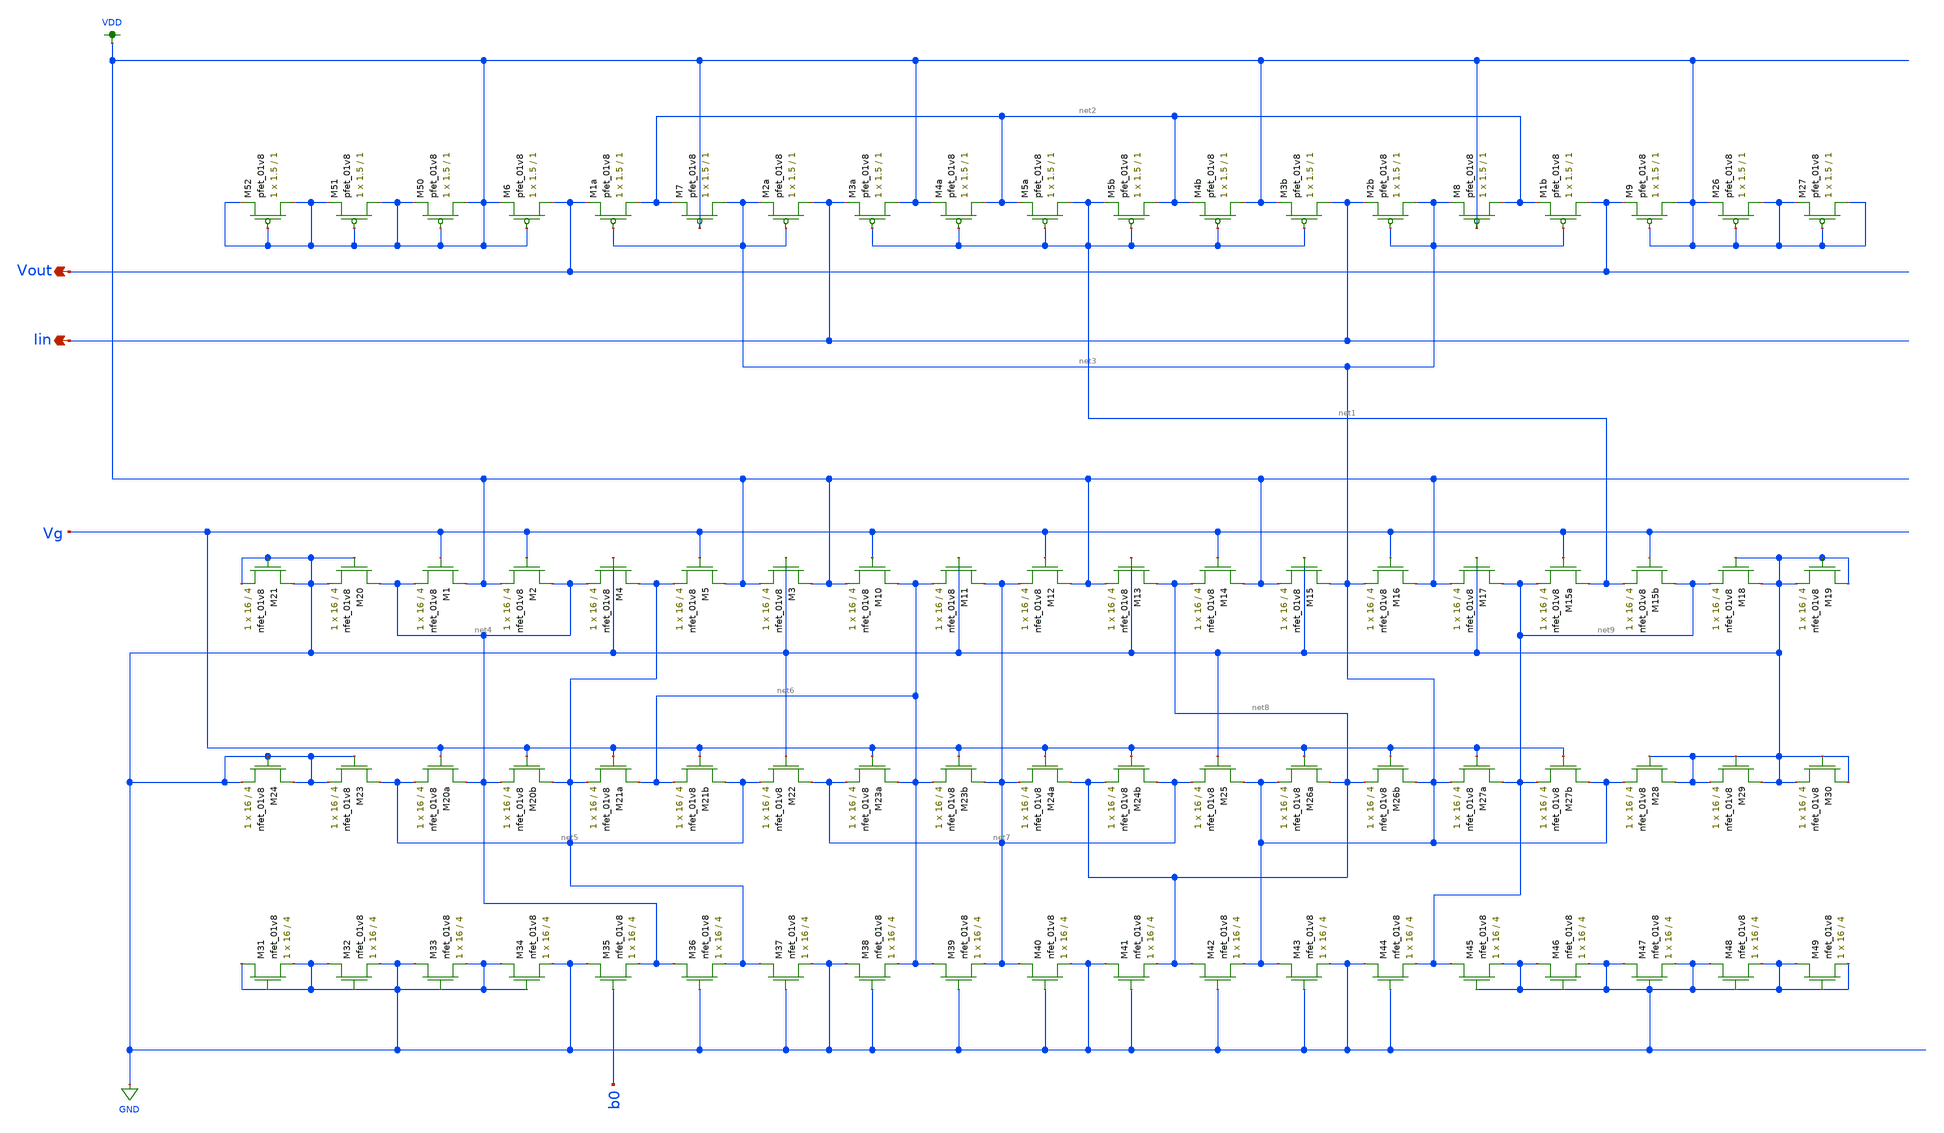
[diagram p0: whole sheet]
** sch_path: schematic/LDS/low-voltage_super-wilson.sch
**.subckt low-voltage_super-wilson Vout Iin
*.opin Vout
*.opin Iin
XM7 net3 VDD net2 VDD sky130_fd_pr__pfet_01v8 L=1 W=1.5 nf=1 ad='int((nf+1)/2) * W/nf * 0.29' as='int((nf+2)/2) * W/nf * 0.29'
+ pd='2*int((nf+1)/2) * (W/nf + 0.29)' ps='2*int((nf+2)/2) * (W/nf + 0.29)' nrd='0.29 / W' nrs='0.29 / W'
+ sa=0 sb=0 sd=0 mult=1 m=1
XM2a Iin net3 net3 VDD sky130_fd_pr__pfet_01v8 L=1 W=1.5 nf=1 ad='int((nf+1)/2) * W/nf * 0.29' as='int((nf+2)/2) * W/nf * 0.29'
+ pd='2*int((nf+1)/2) * (W/nf + 0.29)' ps='2*int((nf+2)/2) * (W/nf + 0.29)' nrd='0.29 / W' nrs='0.29 / W'
+ sa=0 sb=0 sd=0 mult=1 m=1
XM3a VDD net1 Iin VDD sky130_fd_pr__pfet_01v8 L=1 W=1.5 nf=1 ad='int((nf+1)/2) * W/nf * 0.29' as='int((nf+2)/2) * W/nf * 0.29'
+ pd='2*int((nf+1)/2) * (W/nf + 0.29)' ps='2*int((nf+2)/2) * (W/nf + 0.29)' nrd='0.29 / W' nrs='0.29 / W'
+ sa=0 sb=0 sd=0 mult=1 m=1
XM4a net2 net1 VDD VDD sky130_fd_pr__pfet_01v8 L=1 W=1.5 nf=1 ad='int((nf+1)/2) * W/nf * 0.29' as='int((nf+2)/2) * W/nf * 0.29'
+ pd='2*int((nf+1)/2) * (W/nf + 0.29)' ps='2*int((nf+2)/2) * (W/nf + 0.29)' nrd='0.29 / W' nrs='0.29 / W'
+ sa=0 sb=0 sd=0 mult=1 m=1
XM5a net1 net1 net2 VDD sky130_fd_pr__pfet_01v8 L=1 W=1.5 nf=1 ad='int((nf+1)/2) * W/nf * 0.29' as='int((nf+2)/2) * W/nf * 0.29'
+ pd='2*int((nf+1)/2) * (W/nf + 0.29)' ps='2*int((nf+2)/2) * (W/nf + 0.29)' nrd='0.29 / W' nrs='0.29 / W'
+ sa=0 sb=0 sd=0 mult=1 m=1
XM5b net2 net1 net1 VDD sky130_fd_pr__pfet_01v8 L=1 W=1.5 nf=1 ad='int((nf+1)/2) * W/nf * 0.29' as='int((nf+2)/2) * W/nf * 0.29'
+ pd='2*int((nf+1)/2) * (W/nf + 0.29)' ps='2*int((nf+2)/2) * (W/nf + 0.29)' nrd='0.29 / W' nrs='0.29 / W'
+ sa=0 sb=0 sd=0 mult=1 m=1
XM4b VDD net1 net2 VDD sky130_fd_pr__pfet_01v8 L=1 W=1.5 nf=1 ad='int((nf+1)/2) * W/nf * 0.29' as='int((nf+2)/2) * W/nf * 0.29'
+ pd='2*int((nf+1)/2) * (W/nf + 0.29)' ps='2*int((nf+2)/2) * (W/nf + 0.29)' nrd='0.29 / W' nrs='0.29 / W'
+ sa=0 sb=0 sd=0 mult=1 m=1
XM3b Iin net1 VDD VDD sky130_fd_pr__pfet_01v8 L=1 W=1.5 nf=1 ad='int((nf+1)/2) * W/nf * 0.29' as='int((nf+2)/2) * W/nf * 0.29'
+ pd='2*int((nf+1)/2) * (W/nf + 0.29)' ps='2*int((nf+2)/2) * (W/nf + 0.29)' nrd='0.29 / W' nrs='0.29 / W'
+ sa=0 sb=0 sd=0 mult=1 m=1
XM2b net3 net3 Iin VDD sky130_fd_pr__pfet_01v8 L=1 W=1.5 nf=1 ad='int((nf+1)/2) * W/nf * 0.29' as='int((nf+2)/2) * W/nf * 0.29'
+ pd='2*int((nf+1)/2) * (W/nf + 0.29)' ps='2*int((nf+2)/2) * (W/nf + 0.29)' nrd='0.29 / W' nrs='0.29 / W'
+ sa=0 sb=0 sd=0 mult=1 m=1
XM8 net2 VDD net3 VDD sky130_fd_pr__pfet_01v8 L=1 W=1.5 nf=1 ad='int((nf+1)/2) * W/nf * 0.29' as='int((nf+2)/2) * W/nf * 0.29'
+ pd='2*int((nf+1)/2) * (W/nf + 0.29)' ps='2*int((nf+2)/2) * (W/nf + 0.29)' nrd='0.29 / W' nrs='0.29 / W'
+ sa=0 sb=0 sd=0 mult=1 m=1
XM1a net2 net3 Vout VDD sky130_fd_pr__pfet_01v8 L=1 W=1.5 nf=1 ad='int((nf+1)/2) * W/nf * 0.29' as='int((nf+2)/2) * W/nf * 0.29'
+ pd='2*int((nf+1)/2) * (W/nf + 0.29)' ps='2*int((nf+2)/2) * (W/nf + 0.29)' nrd='0.29 / W' nrs='0.29 / W'
+ sa=0 sb=0 sd=0 mult=1 m=1
XM1b Vout net3 net2 VDD sky130_fd_pr__pfet_01v8 L=1 W=1.5 nf=1 ad='int((nf+1)/2) * W/nf * 0.29' as='int((nf+2)/2) * W/nf * 0.29'
+ pd='2*int((nf+1)/2) * (W/nf + 0.29)' ps='2*int((nf+2)/2) * (W/nf + 0.29)' nrd='0.29 / W' nrs='0.29 / W'
+ sa=0 sb=0 sd=0 mult=1 m=1
XM6 Vout VDD VDD VDD sky130_fd_pr__pfet_01v8 L=1 W=1.5 nf=1 ad='int((nf+1)/2) * W/nf * 0.29' as='int((nf+2)/2) * W/nf * 0.29'
+ pd='2*int((nf+1)/2) * (W/nf + 0.29)' ps='2*int((nf+2)/2) * (W/nf + 0.29)' nrd='0.29 / W' nrs='0.29 / W'
+ sa=0 sb=0 sd=0 mult=1 m=1
XM9 VDD VDD Vout VDD sky130_fd_pr__pfet_01v8 L=1 W=1.5 nf=1 ad='int((nf+1)/2) * W/nf * 0.29' as='int((nf+2)/2) * W/nf * 0.29'
+ pd='2*int((nf+1)/2) * (W/nf + 0.29)' ps='2*int((nf+2)/2) * (W/nf + 0.29)' nrd='0.29 / W' nrs='0.29 / W'
+ sa=0 sb=0 sd=0 mult=1 m=1
XM1 VDD Vg net4 GND sky130_fd_pr__nfet_01v8 L=4 W=16 nf=1 ad='int((nf+1)/2) * W/nf * 0.29' as='int((nf+2)/2) * W/nf * 0.29'
+ pd='2*int((nf+1)/2) * (W/nf + 0.29)' ps='2*int((nf+2)/2) * (W/nf + 0.29)' nrd='0.29 / W' nrs='0.29 / W'
+ sa=0 sb=0 sd=0 mult=1 m=1
XM2 net4 Vg VDD GND sky130_fd_pr__nfet_01v8 L=4 W=16 nf=1 ad='int((nf+1)/2) * W/nf * 0.29' as='int((nf+2)/2) * W/nf * 0.29'
+ pd='2*int((nf+1)/2) * (W/nf + 0.29)' ps='2*int((nf+2)/2) * (W/nf + 0.29)' nrd='0.29 / W' nrs='0.29 / W'
+ sa=0 sb=0 sd=0 mult=1 m=1
XM4 net5 GND net4 GND sky130_fd_pr__nfet_01v8 L=4 W=16 nf=1 ad='int((nf+1)/2) * W/nf * 0.29' as='int((nf+2)/2) * W/nf * 0.29'
+ pd='2*int((nf+1)/2) * (W/nf + 0.29)' ps='2*int((nf+2)/2) * (W/nf + 0.29)' nrd='0.29 / W' nrs='0.29 / W'
+ sa=0 sb=0 sd=0 mult=1 m=1
XM5 VDD Vg net5 GND sky130_fd_pr__nfet_01v8 L=4 W=16 nf=1 ad='int((nf+1)/2) * W/nf * 0.29' as='int((nf+2)/2) * W/nf * 0.29'
+ pd='2*int((nf+1)/2) * (W/nf + 0.29)' ps='2*int((nf+2)/2) * (W/nf + 0.29)' nrd='0.29 / W' nrs='0.29 / W'
+ sa=0 sb=0 sd=0 mult=1 m=1
XM3 VDD GND VDD GND sky130_fd_pr__nfet_01v8 L=4 W=16 nf=1 ad='int((nf+1)/2) * W/nf * 0.29' as='int((nf+2)/2) * W/nf * 0.29'
+ pd='2*int((nf+1)/2) * (W/nf + 0.29)' ps='2*int((nf+2)/2) * (W/nf + 0.29)' nrd='0.29 / W' nrs='0.29 / W'
+ sa=0 sb=0 sd=0 mult=1 m=1
XM10 net6 Vg VDD GND sky130_fd_pr__nfet_01v8 L=4 W=16 nf=1 ad='int((nf+1)/2) * W/nf * 0.29' as='int((nf+2)/2) * W/nf * 0.29'
+ pd='2*int((nf+1)/2) * (W/nf + 0.29)' ps='2*int((nf+2)/2) * (W/nf + 0.29)' nrd='0.29 / W' nrs='0.29 / W'
+ sa=0 sb=0 sd=0 mult=1 m=1
XM11 net7 GND net6 GND sky130_fd_pr__nfet_01v8 L=4 W=16 nf=1 ad='int((nf+1)/2) * W/nf * 0.29' as='int((nf+2)/2) * W/nf * 0.29'
+ pd='2*int((nf+1)/2) * (W/nf + 0.29)' ps='2*int((nf+2)/2) * (W/nf + 0.29)' nrd='0.29 / W' nrs='0.29 / W'
+ sa=0 sb=0 sd=0 mult=1 m=1
XM12 VDD Vg net7 GND sky130_fd_pr__nfet_01v8 L=4 W=16 nf=1 ad='int((nf+1)/2) * W/nf * 0.29' as='int((nf+2)/2) * W/nf * 0.29'
+ pd='2*int((nf+1)/2) * (W/nf + 0.29)' ps='2*int((nf+2)/2) * (W/nf + 0.29)' nrd='0.29 / W' nrs='0.29 / W'
+ sa=0 sb=0 sd=0 mult=1 m=1
XM13 net8 GND VDD GND sky130_fd_pr__nfet_01v8 L=4 W=16 nf=1 ad='int((nf+1)/2) * W/nf * 0.29' as='int((nf+2)/2) * W/nf * 0.29'
+ pd='2*int((nf+1)/2) * (W/nf + 0.29)' ps='2*int((nf+2)/2) * (W/nf + 0.29)' nrd='0.29 / W' nrs='0.29 / W'
+ sa=0 sb=0 sd=0 mult=1 m=1
XM14 VDD Vg net8 GND sky130_fd_pr__nfet_01v8 L=4 W=16 nf=1 ad='int((nf+1)/2) * W/nf * 0.29' as='int((nf+2)/2) * W/nf * 0.29'
+ pd='2*int((nf+1)/2) * (W/nf + 0.29)' ps='2*int((nf+2)/2) * (W/nf + 0.29)' nrd='0.29 / W' nrs='0.29 / W'
+ sa=0 sb=0 sd=0 mult=1 m=1
XM15 net3 GND VDD GND sky130_fd_pr__nfet_01v8 L=4 W=16 nf=1 ad='int((nf+1)/2) * W/nf * 0.29' as='int((nf+2)/2) * W/nf * 0.29'
+ pd='2*int((nf+1)/2) * (W/nf + 0.29)' ps='2*int((nf+2)/2) * (W/nf + 0.29)' nrd='0.29 / W' nrs='0.29 / W'
+ sa=0 sb=0 sd=0 mult=1 m=1
XM16 VDD Vg net3 GND sky130_fd_pr__nfet_01v8 L=4 W=16 nf=1 ad='int((nf+1)/2) * W/nf * 0.29' as='int((nf+2)/2) * W/nf * 0.29'
+ pd='2*int((nf+1)/2) * (W/nf + 0.29)' ps='2*int((nf+2)/2) * (W/nf + 0.29)' nrd='0.29 / W' nrs='0.29 / W'
+ sa=0 sb=0 sd=0 mult=1 m=1
XM17 net9 GND VDD GND sky130_fd_pr__nfet_01v8 L=4 W=16 nf=1 ad='int((nf+1)/2) * W/nf * 0.29' as='int((nf+2)/2) * W/nf * 0.29'
+ pd='2*int((nf+1)/2) * (W/nf + 0.29)' ps='2*int((nf+2)/2) * (W/nf + 0.29)' nrd='0.29 / W' nrs='0.29 / W'
+ sa=0 sb=0 sd=0 mult=1 m=1
XM15a net1 Vg net9 GND sky130_fd_pr__nfet_01v8 L=4 W=16 nf=1 ad='int((nf+1)/2) * W/nf * 0.29' as='int((nf+2)/2) * W/nf * 0.29'
+ pd='2*int((nf+1)/2) * (W/nf + 0.29)' ps='2*int((nf+2)/2) * (W/nf + 0.29)' nrd='0.29 / W' nrs='0.29 / W'
+ sa=0 sb=0 sd=0 mult=1 m=1
XM15b net9 Vg net1 GND sky130_fd_pr__nfet_01v8 L=4 W=16 nf=1 ad='int((nf+1)/2) * W/nf * 0.29' as='int((nf+2)/2) * W/nf * 0.29'
+ pd='2*int((nf+1)/2) * (W/nf + 0.29)' ps='2*int((nf+2)/2) * (W/nf + 0.29)' nrd='0.29 / W' nrs='0.29 / W'
+ sa=0 sb=0 sd=0 mult=1 m=1
XM20a net4 Vg net5 GND sky130_fd_pr__nfet_01v8 L=4 W=16 nf=1 ad='int((nf+1)/2) * W/nf * 0.29' as='int((nf+2)/2) * W/nf * 0.29'
+ pd='2*int((nf+1)/2) * (W/nf + 0.29)' ps='2*int((nf+2)/2) * (W/nf + 0.29)' nrd='0.29 / W' nrs='0.29 / W'
+ sa=0 sb=0 sd=0 mult=1 m=1
XM20b net5 Vg net4 GND sky130_fd_pr__nfet_01v8 L=4 W=16 nf=1 ad='int((nf+1)/2) * W/nf * 0.29' as='int((nf+2)/2) * W/nf * 0.29'
+ pd='2*int((nf+1)/2) * (W/nf + 0.29)' ps='2*int((nf+2)/2) * (W/nf + 0.29)' nrd='0.29 / W' nrs='0.29 / W'
+ sa=0 sb=0 sd=0 mult=1 m=1
XM21a net6 Vg net5 GND sky130_fd_pr__nfet_01v8 L=4 W=16 nf=1 ad='int((nf+1)/2) * W/nf * 0.29' as='int((nf+2)/2) * W/nf * 0.29'
+ pd='2*int((nf+1)/2) * (W/nf + 0.29)' ps='2*int((nf+2)/2) * (W/nf + 0.29)' nrd='0.29 / W' nrs='0.29 / W'
+ sa=0 sb=0 sd=0 mult=1 m=1
XM21b net5 Vg net6 GND sky130_fd_pr__nfet_01v8 L=4 W=16 nf=1 ad='int((nf+1)/2) * W/nf * 0.29' as='int((nf+2)/2) * W/nf * 0.29'
+ pd='2*int((nf+1)/2) * (W/nf + 0.29)' ps='2*int((nf+2)/2) * (W/nf + 0.29)' nrd='0.29 / W' nrs='0.29 / W'
+ sa=0 sb=0 sd=0 mult=1 m=1
XM22 net7 GND net5 GND sky130_fd_pr__nfet_01v8 L=4 W=16 nf=1 ad='int((nf+1)/2) * W/nf * 0.29' as='int((nf+2)/2) * W/nf * 0.29'
+ pd='2*int((nf+1)/2) * (W/nf + 0.29)' ps='2*int((nf+2)/2) * (W/nf + 0.29)' nrd='0.29 / W' nrs='0.29 / W'
+ sa=0 sb=0 sd=0 mult=1 m=1
XM23a net6 Vg net7 GND sky130_fd_pr__nfet_01v8 L=4 W=16 nf=1 ad='int((nf+1)/2) * W/nf * 0.29' as='int((nf+2)/2) * W/nf * 0.29'
+ pd='2*int((nf+1)/2) * (W/nf + 0.29)' ps='2*int((nf+2)/2) * (W/nf + 0.29)' nrd='0.29 / W' nrs='0.29 / W'
+ sa=0 sb=0 sd=0 mult=1 m=1
XM23b net7 Vg net6 GND sky130_fd_pr__nfet_01v8 L=4 W=16 nf=1 ad='int((nf+1)/2) * W/nf * 0.29' as='int((nf+2)/2) * W/nf * 0.29'
+ pd='2*int((nf+1)/2) * (W/nf + 0.29)' ps='2*int((nf+2)/2) * (W/nf + 0.29)' nrd='0.29 / W' nrs='0.29 / W'
+ sa=0 sb=0 sd=0 mult=1 m=1
XM24a net8 Vg net7 GND sky130_fd_pr__nfet_01v8 L=4 W=16 nf=1 ad='int((nf+1)/2) * W/nf * 0.29' as='int((nf+2)/2) * W/nf * 0.29'
+ pd='2*int((nf+1)/2) * (W/nf + 0.29)' ps='2*int((nf+2)/2) * (W/nf + 0.29)' nrd='0.29 / W' nrs='0.29 / W'
+ sa=0 sb=0 sd=0 mult=1 m=1
XM24b net7 Vg net8 GND sky130_fd_pr__nfet_01v8 L=4 W=16 nf=1 ad='int((nf+1)/2) * W/nf * 0.29' as='int((nf+2)/2) * W/nf * 0.29'
+ pd='2*int((nf+1)/2) * (W/nf + 0.29)' ps='2*int((nf+2)/2) * (W/nf + 0.29)' nrd='0.29 / W' nrs='0.29 / W'
+ sa=0 sb=0 sd=0 mult=1 m=1
XM25 net3 GND net7 GND sky130_fd_pr__nfet_01v8 L=4 W=16 nf=1 ad='int((nf+1)/2) * W/nf * 0.29' as='int((nf+2)/2) * W/nf * 0.29'
+ pd='2*int((nf+1)/2) * (W/nf + 0.29)' ps='2*int((nf+2)/2) * (W/nf + 0.29)' nrd='0.29 / W' nrs='0.29 / W'
+ sa=0 sb=0 sd=0 mult=1 m=1
XM26a net8 Vg net3 GND sky130_fd_pr__nfet_01v8 L=4 W=16 nf=1 ad='int((nf+1)/2) * W/nf * 0.29' as='int((nf+2)/2) * W/nf * 0.29'
+ pd='2*int((nf+1)/2) * (W/nf + 0.29)' ps='2*int((nf+2)/2) * (W/nf + 0.29)' nrd='0.29 / W' nrs='0.29 / W'
+ sa=0 sb=0 sd=0 mult=1 m=1
XM26b net3 Vg net8 GND sky130_fd_pr__nfet_01v8 L=4 W=16 nf=1 ad='int((nf+1)/2) * W/nf * 0.29' as='int((nf+2)/2) * W/nf * 0.29'
+ pd='2*int((nf+1)/2) * (W/nf + 0.29)' ps='2*int((nf+2)/2) * (W/nf + 0.29)' nrd='0.29 / W' nrs='0.29 / W'
+ sa=0 sb=0 sd=0 mult=1 m=1
XM27a net9 Vg net3 GND sky130_fd_pr__nfet_01v8 L=4 W=16 nf=1 ad='int((nf+1)/2) * W/nf * 0.29' as='int((nf+2)/2) * W/nf * 0.29'
+ pd='2*int((nf+1)/2) * (W/nf + 0.29)' ps='2*int((nf+2)/2) * (W/nf + 0.29)' nrd='0.29 / W' nrs='0.29 / W'
+ sa=0 sb=0 sd=0 mult=1 m=1
XM27b net3 Vg net9 GND sky130_fd_pr__nfet_01v8 L=4 W=16 nf=1 ad='int((nf+1)/2) * W/nf * 0.29' as='int((nf+2)/2) * W/nf * 0.29'
+ pd='2*int((nf+1)/2) * (W/nf + 0.29)' ps='2*int((nf+2)/2) * (W/nf + 0.29)' nrd='0.29 / W' nrs='0.29 / W'
+ sa=0 sb=0 sd=0 mult=1 m=1
XM35 GND b0 net4 GND sky130_fd_pr__nfet_01v8 L=4 W=16 nf=1 ad='int((nf+1)/2) * W/nf * 0.29' as='int((nf+2)/2) * W/nf * 0.29'
+ pd='2*int((nf+1)/2) * (W/nf + 0.29)' ps='2*int((nf+2)/2) * (W/nf + 0.29)' nrd='0.29 / W' nrs='0.29 / W'
+ sa=0 sb=0 sd=0 mult=1 m=1
XM36 net4 GND net5 GND sky130_fd_pr__nfet_01v8 L=4 W=16 nf=1 ad='int((nf+1)/2) * W/nf * 0.29' as='int((nf+2)/2) * W/nf * 0.29'
+ pd='2*int((nf+1)/2) * (W/nf + 0.29)' ps='2*int((nf+2)/2) * (W/nf + 0.29)' nrd='0.29 / W' nrs='0.29 / W'
+ sa=0 sb=0 sd=0 mult=1 m=1
XM37 net5 GND GND GND sky130_fd_pr__nfet_01v8 L=4 W=16 nf=1 ad='int((nf+1)/2) * W/nf * 0.29' as='int((nf+2)/2) * W/nf * 0.29'
+ pd='2*int((nf+1)/2) * (W/nf + 0.29)' ps='2*int((nf+2)/2) * (W/nf + 0.29)' nrd='0.29 / W' nrs='0.29 / W'
+ sa=0 sb=0 sd=0 mult=1 m=1
XM38 GND GND net6 GND sky130_fd_pr__nfet_01v8 L=4 W=16 nf=1 ad='int((nf+1)/2) * W/nf * 0.29' as='int((nf+2)/2) * W/nf * 0.29'
+ pd='2*int((nf+1)/2) * (W/nf + 0.29)' ps='2*int((nf+2)/2) * (W/nf + 0.29)' nrd='0.29 / W' nrs='0.29 / W'
+ sa=0 sb=0 sd=0 mult=1 m=1
XM39 net6 GND net7 GND sky130_fd_pr__nfet_01v8 L=4 W=16 nf=1 ad='int((nf+1)/2) * W/nf * 0.29' as='int((nf+2)/2) * W/nf * 0.29'
+ pd='2*int((nf+1)/2) * (W/nf + 0.29)' ps='2*int((nf+2)/2) * (W/nf + 0.29)' nrd='0.29 / W' nrs='0.29 / W'
+ sa=0 sb=0 sd=0 mult=1 m=1
XM40 net7 GND GND GND sky130_fd_pr__nfet_01v8 L=4 W=16 nf=1 ad='int((nf+1)/2) * W/nf * 0.29' as='int((nf+2)/2) * W/nf * 0.29'
+ pd='2*int((nf+1)/2) * (W/nf + 0.29)' ps='2*int((nf+2)/2) * (W/nf + 0.29)' nrd='0.29 / W' nrs='0.29 / W'
+ sa=0 sb=0 sd=0 mult=1 m=1
XM41 GND GND net8 GND sky130_fd_pr__nfet_01v8 L=4 W=16 nf=1 ad='int((nf+1)/2) * W/nf * 0.29' as='int((nf+2)/2) * W/nf * 0.29'
+ pd='2*int((nf+1)/2) * (W/nf + 0.29)' ps='2*int((nf+2)/2) * (W/nf + 0.29)' nrd='0.29 / W' nrs='0.29 / W'
+ sa=0 sb=0 sd=0 mult=1 m=1
XM42 net8 GND net3 GND sky130_fd_pr__nfet_01v8 L=4 W=16 nf=1 ad='int((nf+1)/2) * W/nf * 0.29' as='int((nf+2)/2) * W/nf * 0.29'
+ pd='2*int((nf+1)/2) * (W/nf + 0.29)' ps='2*int((nf+2)/2) * (W/nf + 0.29)' nrd='0.29 / W' nrs='0.29 / W'
+ sa=0 sb=0 sd=0 mult=1 m=1
XM43 net3 GND GND GND sky130_fd_pr__nfet_01v8 L=4 W=16 nf=1 ad='int((nf+1)/2) * W/nf * 0.29' as='int((nf+2)/2) * W/nf * 0.29'
+ pd='2*int((nf+1)/2) * (W/nf + 0.29)' ps='2*int((nf+2)/2) * (W/nf + 0.29)' nrd='0.29 / W' nrs='0.29 / W'
+ sa=0 sb=0 sd=0 mult=1 m=1
XM44 GND GND net9 GND sky130_fd_pr__nfet_01v8 L=4 W=16 nf=1 ad='int((nf+1)/2) * W/nf * 0.29' as='int((nf+2)/2) * W/nf * 0.29'
+ pd='2*int((nf+1)/2) * (W/nf + 0.29)' ps='2*int((nf+2)/2) * (W/nf + 0.29)' nrd='0.29 / W' nrs='0.29 / W'
+ sa=0 sb=0 sd=0 mult=1 m=1
XM18 GND GND net9 GND sky130_fd_pr__nfet_01v8 L=4 W=16 nf=1 ad='int((nf+1)/2) * W/nf * 0.29' as='int((nf+2)/2) * W/nf * 0.29'
+ pd='2*int((nf+1)/2) * (W/nf + 0.29)' ps='2*int((nf+2)/2) * (W/nf + 0.29)' nrd='0.29 / W' nrs='0.29 / W'
+ sa=0 sb=0 sd=0 mult=1 m=1
XM19 GND GND GND GND sky130_fd_pr__nfet_01v8 L=4 W=16 nf=1 ad='int((nf+1)/2) * W/nf * 0.29' as='int((nf+2)/2) * W/nf * 0.29'
+ pd='2*int((nf+1)/2) * (W/nf + 0.29)' ps='2*int((nf+2)/2) * (W/nf + 0.29)' nrd='0.29 / W' nrs='0.29 / W'
+ sa=0 sb=0 sd=0 mult=1 m=1
XM20 net4 GND GND GND sky130_fd_pr__nfet_01v8 L=4 W=16 nf=1 ad='int((nf+1)/2) * W/nf * 0.29' as='int((nf+2)/2) * W/nf * 0.29'
+ pd='2*int((nf+1)/2) * (W/nf + 0.29)' ps='2*int((nf+2)/2) * (W/nf + 0.29)' nrd='0.29 / W' nrs='0.29 / W'
+ sa=0 sb=0 sd=0 mult=1 m=1
XM21 GND GND GND GND sky130_fd_pr__nfet_01v8 L=4 W=16 nf=1 ad='int((nf+1)/2) * W/nf * 0.29' as='int((nf+2)/2) * W/nf * 0.29'
+ pd='2*int((nf+1)/2) * (W/nf + 0.29)' ps='2*int((nf+2)/2) * (W/nf + 0.29)' nrd='0.29 / W' nrs='0.29 / W'
+ sa=0 sb=0 sd=0 mult=1 m=1
XM23 net5 GND GND GND sky130_fd_pr__nfet_01v8 L=4 W=16 nf=1 ad='int((nf+1)/2) * W/nf * 0.29' as='int((nf+2)/2) * W/nf * 0.29'
+ pd='2*int((nf+1)/2) * (W/nf + 0.29)' ps='2*int((nf+2)/2) * (W/nf + 0.29)' nrd='0.29 / W' nrs='0.29 / W'
+ sa=0 sb=0 sd=0 mult=1 m=1
XM24 GND GND GND GND sky130_fd_pr__nfet_01v8 L=4 W=16 nf=1 ad='int((nf+1)/2) * W/nf * 0.29' as='int((nf+2)/2) * W/nf * 0.29'
+ pd='2*int((nf+1)/2) * (W/nf + 0.29)' ps='2*int((nf+2)/2) * (W/nf + 0.29)' nrd='0.29 / W' nrs='0.29 / W'
+ sa=0 sb=0 sd=0 mult=1 m=1
XM28 GND GND net3 GND sky130_fd_pr__nfet_01v8 L=4 W=16 nf=1 ad='int((nf+1)/2) * W/nf * 0.29' as='int((nf+2)/2) * W/nf * 0.29'
+ pd='2*int((nf+1)/2) * (W/nf + 0.29)' ps='2*int((nf+2)/2) * (W/nf + 0.29)' nrd='0.29 / W' nrs='0.29 / W'
+ sa=0 sb=0 sd=0 mult=1 m=1
XM29 GND GND GND GND sky130_fd_pr__nfet_01v8 L=4 W=16 nf=1 ad='int((nf+1)/2) * W/nf * 0.29' as='int((nf+2)/2) * W/nf * 0.29'
+ pd='2*int((nf+1)/2) * (W/nf + 0.29)' ps='2*int((nf+2)/2) * (W/nf + 0.29)' nrd='0.29 / W' nrs='0.29 / W'
+ sa=0 sb=0 sd=0 mult=1 m=1
XM30 GND GND GND GND sky130_fd_pr__nfet_01v8 L=4 W=16 nf=1 ad='int((nf+1)/2) * W/nf * 0.29' as='int((nf+2)/2) * W/nf * 0.29'
+ pd='2*int((nf+1)/2) * (W/nf + 0.29)' ps='2*int((nf+2)/2) * (W/nf + 0.29)' nrd='0.29 / W' nrs='0.29 / W'
+ sa=0 sb=0 sd=0 mult=1 m=1
XM45 net9 GND GND GND sky130_fd_pr__nfet_01v8 L=4 W=16 nf=1 ad='int((nf+1)/2) * W/nf * 0.29' as='int((nf+2)/2) * W/nf * 0.29'
+ pd='2*int((nf+1)/2) * (W/nf + 0.29)' ps='2*int((nf+2)/2) * (W/nf + 0.29)' nrd='0.29 / W' nrs='0.29 / W'
+ sa=0 sb=0 sd=0 mult=1 m=1
XM46 GND GND GND GND sky130_fd_pr__nfet_01v8 L=4 W=16 nf=1 ad='int((nf+1)/2) * W/nf * 0.29' as='int((nf+2)/2) * W/nf * 0.29'
+ pd='2*int((nf+1)/2) * (W/nf + 0.29)' ps='2*int((nf+2)/2) * (W/nf + 0.29)' nrd='0.29 / W' nrs='0.29 / W'
+ sa=0 sb=0 sd=0 mult=1 m=1
XM47 GND GND GND GND sky130_fd_pr__nfet_01v8 L=4 W=16 nf=1 ad='int((nf+1)/2) * W/nf * 0.29' as='int((nf+2)/2) * W/nf * 0.29'
+ pd='2*int((nf+1)/2) * (W/nf + 0.29)' ps='2*int((nf+2)/2) * (W/nf + 0.29)' nrd='0.29 / W' nrs='0.29 / W'
+ sa=0 sb=0 sd=0 mult=1 m=1
XM48 GND GND GND GND sky130_fd_pr__nfet_01v8 L=4 W=16 nf=1 ad='int((nf+1)/2) * W/nf * 0.29' as='int((nf+2)/2) * W/nf * 0.29'
+ pd='2*int((nf+1)/2) * (W/nf + 0.29)' ps='2*int((nf+2)/2) * (W/nf + 0.29)' nrd='0.29 / W' nrs='0.29 / W'
+ sa=0 sb=0 sd=0 mult=1 m=1
XM49 GND GND GND GND sky130_fd_pr__nfet_01v8 L=4 W=16 nf=1 ad='int((nf+1)/2) * W/nf * 0.29' as='int((nf+2)/2) * W/nf * 0.29'
+ pd='2*int((nf+1)/2) * (W/nf + 0.29)' ps='2*int((nf+2)/2) * (W/nf + 0.29)' nrd='0.29 / W' nrs='0.29 / W'
+ sa=0 sb=0 sd=0 mult=1 m=1
XM34 GND GND GND GND sky130_fd_pr__nfet_01v8 L=4 W=16 nf=1 ad='int((nf+1)/2) * W/nf * 0.29' as='int((nf+2)/2) * W/nf * 0.29'
+ pd='2*int((nf+1)/2) * (W/nf + 0.29)' ps='2*int((nf+2)/2) * (W/nf + 0.29)' nrd='0.29 / W' nrs='0.29 / W'
+ sa=0 sb=0 sd=0 mult=1 m=1
XM33 GND GND GND GND sky130_fd_pr__nfet_01v8 L=4 W=16 nf=1 ad='int((nf+1)/2) * W/nf * 0.29' as='int((nf+2)/2) * W/nf * 0.29'
+ pd='2*int((nf+1)/2) * (W/nf + 0.29)' ps='2*int((nf+2)/2) * (W/nf + 0.29)' nrd='0.29 / W' nrs='0.29 / W'
+ sa=0 sb=0 sd=0 mult=1 m=1
XM32 GND GND GND GND sky130_fd_pr__nfet_01v8 L=4 W=16 nf=1 ad='int((nf+1)/2) * W/nf * 0.29' as='int((nf+2)/2) * W/nf * 0.29'
+ pd='2*int((nf+1)/2) * (W/nf + 0.29)' ps='2*int((nf+2)/2) * (W/nf + 0.29)' nrd='0.29 / W' nrs='0.29 / W'
+ sa=0 sb=0 sd=0 mult=1 m=1
XM31 GND GND GND GND sky130_fd_pr__nfet_01v8 L=4 W=16 nf=1 ad='int((nf+1)/2) * W/nf * 0.29' as='int((nf+2)/2) * W/nf * 0.29'
+ pd='2*int((nf+1)/2) * (W/nf + 0.29)' ps='2*int((nf+2)/2) * (W/nf + 0.29)' nrd='0.29 / W' nrs='0.29 / W'
+ sa=0 sb=0 sd=0 mult=1 m=1
XM26 VDD VDD VDD VDD sky130_fd_pr__pfet_01v8 L=1 W=1.5 nf=1 ad='int((nf+1)/2) * W/nf * 0.29' as='int((nf+2)/2) * W/nf * 0.29'
+ pd='2*int((nf+1)/2) * (W/nf + 0.29)' ps='2*int((nf+2)/2) * (W/nf + 0.29)' nrd='0.29 / W' nrs='0.29 / W'
+ sa=0 sb=0 sd=0 mult=1 m=1
XM27 VDD VDD VDD VDD sky130_fd_pr__pfet_01v8 L=1 W=1.5 nf=1 ad='int((nf+1)/2) * W/nf * 0.29' as='int((nf+2)/2) * W/nf * 0.29'
+ pd='2*int((nf+1)/2) * (W/nf + 0.29)' ps='2*int((nf+2)/2) * (W/nf + 0.29)' nrd='0.29 / W' nrs='0.29 / W'
+ sa=0 sb=0 sd=0 mult=1 m=1
XM50 VDD VDD VDD VDD sky130_fd_pr__pfet_01v8 L=1 W=1.5 nf=1 ad='int((nf+1)/2) * W/nf * 0.29' as='int((nf+2)/2) * W/nf * 0.29'
+ pd='2*int((nf+1)/2) * (W/nf + 0.29)' ps='2*int((nf+2)/2) * (W/nf + 0.29)' nrd='0.29 / W' nrs='0.29 / W'
+ sa=0 sb=0 sd=0 mult=1 m=1
XM51 VDD VDD VDD VDD sky130_fd_pr__pfet_01v8 L=1 W=1.5 nf=1 ad='int((nf+1)/2) * W/nf * 0.29' as='int((nf+2)/2) * W/nf * 0.29'
+ pd='2*int((nf+1)/2) * (W/nf + 0.29)' ps='2*int((nf+2)/2) * (W/nf + 0.29)' nrd='0.29 / W' nrs='0.29 / W'
+ sa=0 sb=0 sd=0 mult=1 m=1
XM52 VDD VDD VDD VDD sky130_fd_pr__pfet_01v8 L=1 W=1.5 nf=1 ad='int((nf+1)/2) * W/nf * 0.29' as='int((nf+2)/2) * W/nf * 0.29'
+ pd='2*int((nf+1)/2) * (W/nf + 0.29)' ps='2*int((nf+2)/2) * (W/nf + 0.29)' nrd='0.29 / W' nrs='0.29 / W'
+ sa=0 sb=0 sd=0 mult=1 m=1
**.ends
.GLOBAL VDD
.GLOBAL GND
.end
